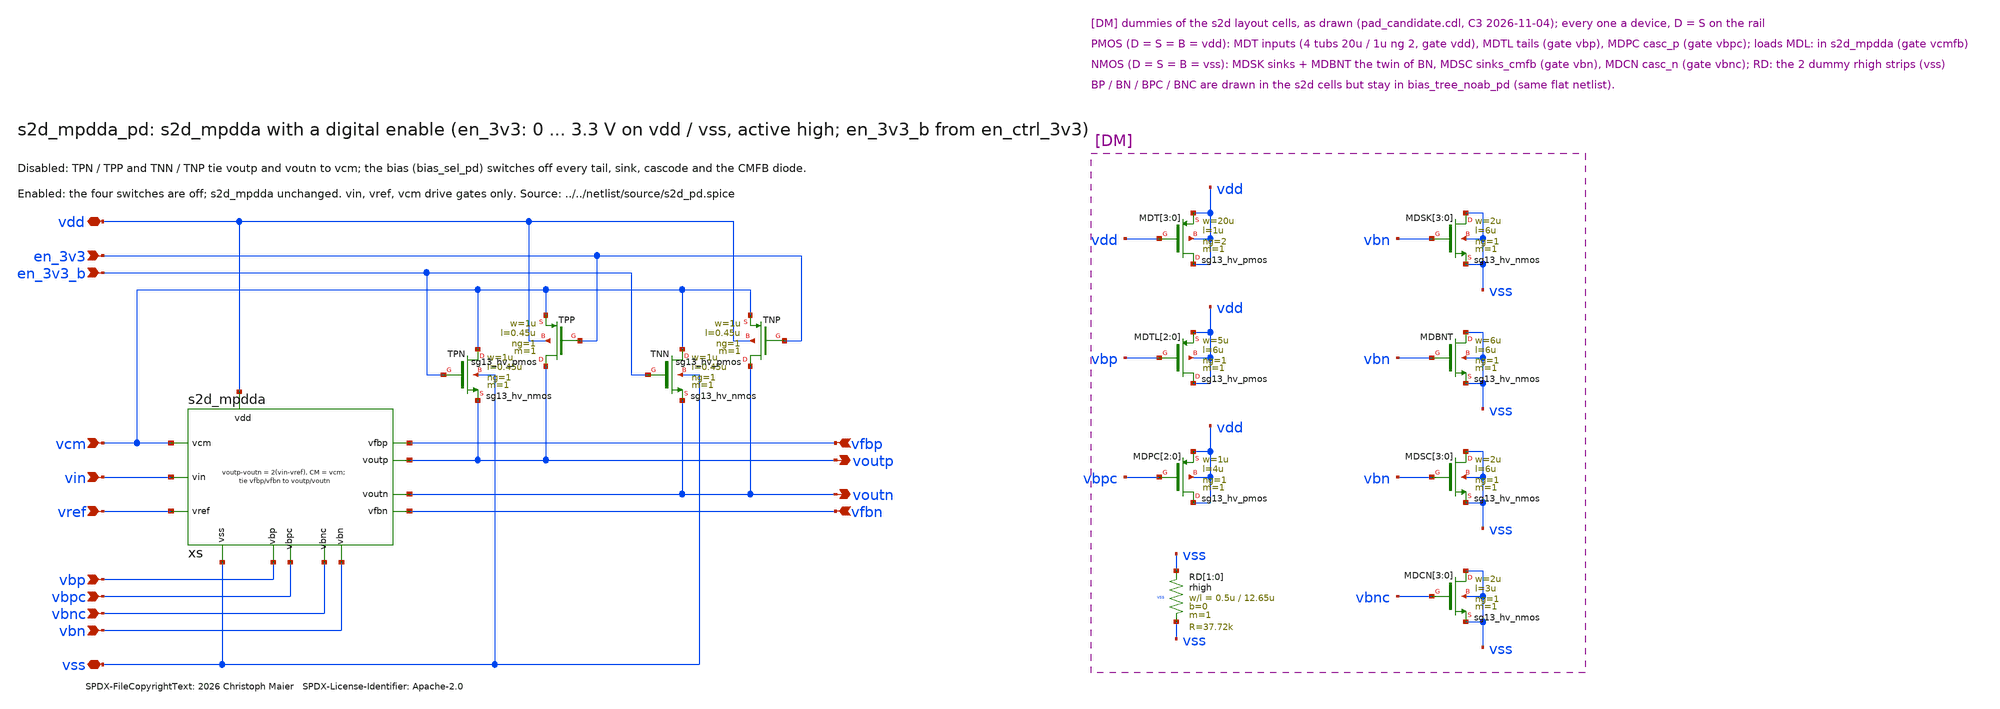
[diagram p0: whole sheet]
** sch_path: macros/sg13cmos5l_IOPadSingle2Diff/schematic/xschem/s2d_mpdda_pd.sch
* SPDX-FileCopyrightText: 2026 Christoph Maier SPDX-License-Identifier: Apache-2.0
**.subckt s2d_mpdda_pd vdd en_3v3 en_3v3_b vin vref vcm vfbp vfbn vbp vbn vbpc vbnc vss voutp voutn
*.iopin vdd
*.ipin en_3v3
*.ipin en_3v3_b
*.ipin vin
*.ipin vref
*.ipin vcm
*.ipin vfbp
*.ipin vfbn
*.ipin vbp
*.ipin vbn
*.ipin vbpc
*.ipin vbnc
*.iopin vss
*.opin voutp
*.opin voutn
xs vdd vss vin vref vcm voutp voutn vfbp vfbn vbp vbn vbpc vbnc s2d_mpdda
XTPN vcm en_3v3_b voutp vss sg13_hv_nmos w=1u l=0.45u ng=1 m=1 mm_ok=1
XTPP voutp en_3v3 vcm vdd sg13_hv_pmos w=1u l=0.45u ng=1 m=1 mm_ok=1
XTNN vcm en_3v3_b voutn vss sg13_hv_nmos w=1u l=0.45u ng=1 m=1 mm_ok=1
XTNP voutn en_3v3 vcm vdd sg13_hv_pmos w=1u l=0.45u ng=1 m=1 mm_ok=1
XMDT[3] vdd vdd vdd vdd sg13_hv_pmos w=20u l=1u ng=2 m=1 mm_ok=1
XMDT[2] vdd vdd vdd vdd sg13_hv_pmos w=20u l=1u ng=2 m=1 mm_ok=1
XMDT[1] vdd vdd vdd vdd sg13_hv_pmos w=20u l=1u ng=2 m=1 mm_ok=1
XMDT[0] vdd vdd vdd vdd sg13_hv_pmos w=20u l=1u ng=2 m=1 mm_ok=1
XMDTL[2] vdd vbp vdd vdd sg13_hv_pmos w=5u l=6u ng=1 m=1 mm_ok=1
XMDTL[1] vdd vbp vdd vdd sg13_hv_pmos w=5u l=6u ng=1 m=1 mm_ok=1
XMDTL[0] vdd vbp vdd vdd sg13_hv_pmos w=5u l=6u ng=1 m=1 mm_ok=1
XMDPC[2] vdd vbpc vdd vdd sg13_hv_pmos w=1u l=4u ng=1 m=1 mm_ok=1
XMDPC[1] vdd vbpc vdd vdd sg13_hv_pmos w=1u l=4u ng=1 m=1 mm_ok=1
XMDPC[0] vdd vbpc vdd vdd sg13_hv_pmos w=1u l=4u ng=1 m=1 mm_ok=1
XRD[1] vss vss vss rhigh w=0.5u l=12.65u m=1 b=0 mm_ok=1
XRD[0] vss vss vss rhigh w=0.5u l=12.65u m=1 b=0 mm_ok=1
XMDSK[3] vss vbn vss vss sg13_hv_nmos w=2u l=6u ng=1 m=1 mm_ok=1
XMDSK[2] vss vbn vss vss sg13_hv_nmos w=2u l=6u ng=1 m=1 mm_ok=1
XMDSK[1] vss vbn vss vss sg13_hv_nmos w=2u l=6u ng=1 m=1 mm_ok=1
XMDSK[0] vss vbn vss vss sg13_hv_nmos w=2u l=6u ng=1 m=1 mm_ok=1
XMDBNT vss vbn vss vss sg13_hv_nmos w=6u l=6u ng=1 m=1 mm_ok=1
XMDSC[3] vss vbn vss vss sg13_hv_nmos w=2u l=6u ng=1 m=1 mm_ok=1
XMDSC[2] vss vbn vss vss sg13_hv_nmos w=2u l=6u ng=1 m=1 mm_ok=1
XMDSC[1] vss vbn vss vss sg13_hv_nmos w=2u l=6u ng=1 m=1 mm_ok=1
XMDSC[0] vss vbn vss vss sg13_hv_nmos w=2u l=6u ng=1 m=1 mm_ok=1
XMDCN[3] vss vbnc vss vss sg13_hv_nmos w=2u l=3u ng=1 m=1 mm_ok=1
XMDCN[2] vss vbnc vss vss sg13_hv_nmos w=2u l=3u ng=1 m=1 mm_ok=1
XMDCN[1] vss vbnc vss vss sg13_hv_nmos w=2u l=3u ng=1 m=1 mm_ok=1
XMDCN[0] vss vbnc vss vss sg13_hv_nmos w=2u l=3u ng=1 m=1 mm_ok=1
**.ends

* expanding   symbol:  s2d_mpdda.sym # of pins=13
** sym_path: macros/sg13cmos5l_IOPadSingle2Diff/schematic/xschem/s2d_mpdda.sym
** sch_path: macros/sg13cmos5l_IOPadSingle2Diff/schematic/xschem/s2d_mpdda.sch
.subckt s2d_mpdda vdd vss vin vref vcm voutp voutn vfbp vfbn vbp vbn vbpc vbnc
*.iopin vdd
*.iopin vss
*.ipin vin
*.ipin vref
*.ipin vcm
*.opin voutp
*.opin voutn
*.ipin vfbp
*.ipin vfbn
*.iopin vbp
*.iopin vbn
*.iopin vbpc
*.iopin vbnc
XA1 x y vin vref vdd vss vbp unit_r2
XA2 x y vin vref vdd vss vbp unit_r2
XF1 x y vcm vfbp vdd vss vbp unit_r2
XF2 x y vfbn vcm vdd vss vbp unit_r2
XLP lp vcmfb vdd vdd sg13_hv_pmos w=24u l=4u ng=4 m=1 mm_ok=1
XLPC voutp vbpc lp vdd sg13_hv_pmos w=30u l=3u ng=2 m=1 mm_ok=1
XCX voutp vbnc x vss sg13_hv_nmos w=30u l=3u ng=2 m=1 mm_ok=1
XSX x vbn vss vss sg13_hv_nmos w=36u l=6u ng=6 m=1 mm_ok=1
XLN ln vcmfb vdd vdd sg13_hv_pmos w=24u l=4u ng=4 m=1 mm_ok=1
XLNC voutn vbpc ln vdd sg13_hv_pmos w=30u l=3u ng=2 m=1 mm_ok=1
XCY voutn vbnc y vss sg13_hv_nmos w=30u l=3u ng=2 m=1 mm_ok=1
XSY y vbn vss vss sg13_hv_nmos w=36u l=6u ng=6 m=1 mm_ok=1
XCLP vss voutp vss vss sg13_hv_nmos w=12u l=12u ng=1 m=1 mm_ok=1
XCLN vss voutn vss vss sg13_hv_nmos w=12u l=12u ng=1 m=1 mm_ok=1
XM1 xc yc vfbp vcm vdd vss vbp unit_r2
XM2 xc yc vfbn vcm vdd vss vbp unit_r2
XD dd vcmfb vdd vdd sg13_hv_pmos w=24u l=4u ng=4 m=1 mm_ok=1
XDC vcmfb vbpc dd vdd sg13_hv_pmos w=30u l=3u ng=2 m=1 mm_ok=1
XCXC vcmfb vbnc xc vss sg13_hv_nmos w=30u l=3u ng=2 m=1 mm_ok=1
XSXC xc vbn vss vss sg13_hv_nmos w=24u l=6u ng=4 m=1 mm_ok=1
XCYC vdd vbnc yc vss sg13_hv_nmos w=30u l=3u ng=2 m=1 mm_ok=1
XSYC yc vbn vss vss sg13_hv_nmos w=24u l=6u ng=4 m=1 mm_ok=1
XMDL[3] vdd vcmfb vdd vdd sg13_hv_pmos w=1u l=4u ng=1 m=1 mm_ok=1
XMDL[2] vdd vcmfb vdd vdd sg13_hv_pmos w=1u l=4u ng=1 m=1 mm_ok=1
XMDL[1] vdd vcmfb vdd vdd sg13_hv_pmos w=1u l=4u ng=1 m=1 mm_ok=1
XMDL[0] vdd vcmfb vdd vdd sg13_hv_pmos w=1u l=4u ng=1 m=1 mm_ok=1
.ends


* expanding   symbol:  unit_r2.sym # of pins=7
** sym_path: sudelbuecher/design_considerations/class_ab_pad_driver/improvements/xschem/unit_r2.sym
** sch_path: sudelbuecher/design_considerations/class_ab_pad_driver/improvements/xschem/unit_r2.sch
.subckt unit_r2 x y gp gn vdd vss vbp
*.opin x
*.opin y
*.ipin gp
*.ipin gn
*.iopin vdd
*.iopin vss
*.ipin vbp
XTa sa vbp vdd vdd sg13_hv_pmos w=5u l=6u ng=1 m=1 mm_ok=1
XTb sb vbp vdd vdd sg13_hv_pmos w=5u l=6u ng=1 m=1 mm_ok=1
XMa y gp sa sa sg13_hv_pmos w=20u l=1u ng=2 m=1 mm_ok=1
XMb x gn sb sb sg13_hv_pmos w=20u l=1u ng=2 m=1 mm_ok=1
XR sa sb vss rhigh w=0.5u l=50.6u m=1 b=0 mm_ok=1
.ends

.end
